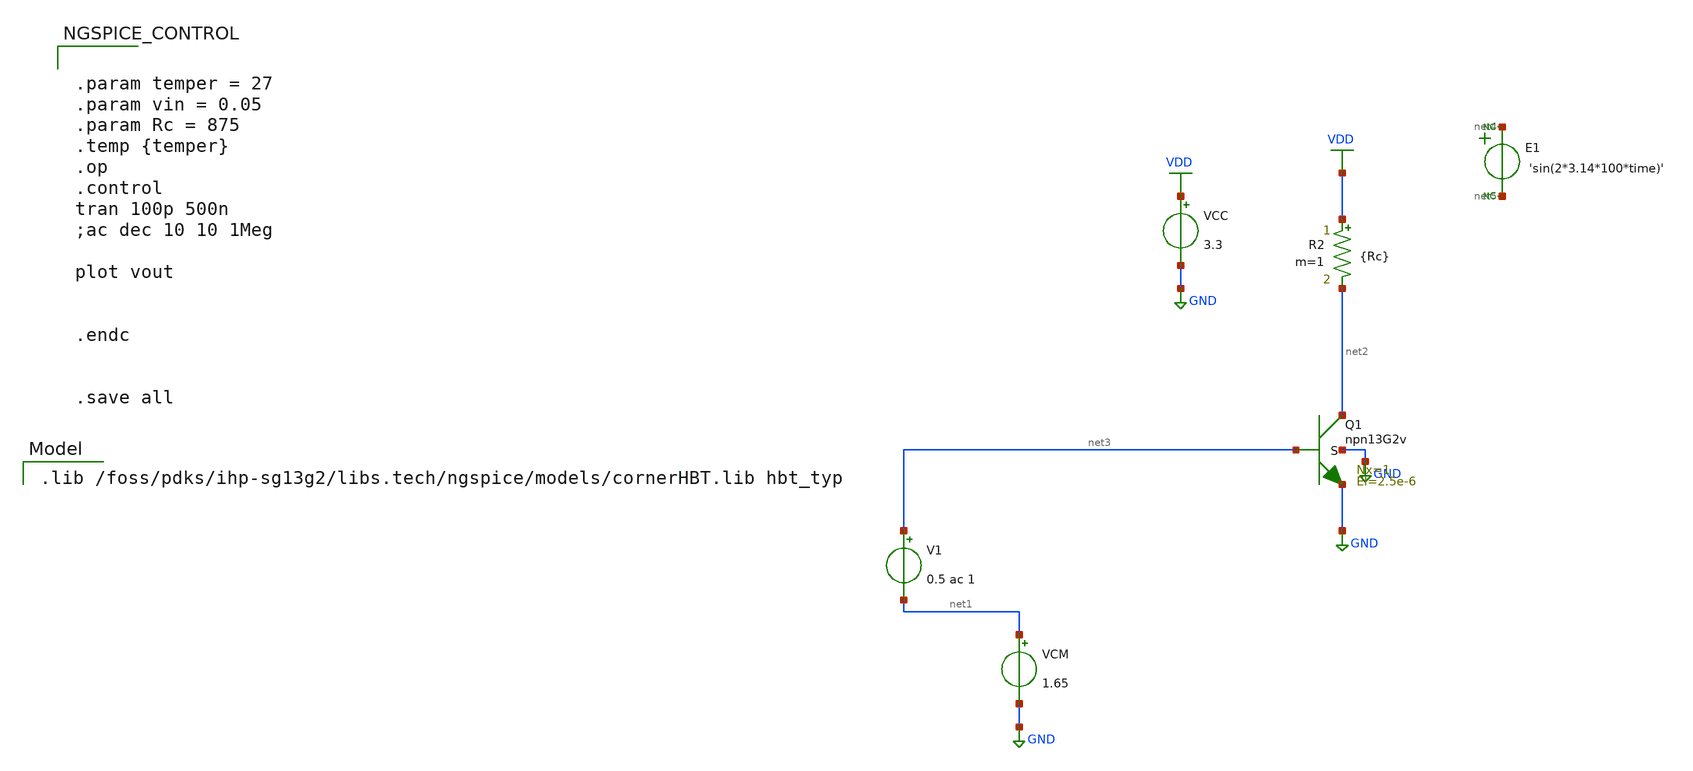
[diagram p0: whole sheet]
** sch_path: data_simu/simulations/LNA_design_ihp_test.sch
**.subckt LNA_design_ihp_test
VCC VDD GND 3.3
R2 VDD net2 {Rc} m=1
VCM net1 GND 1.65
E1 net4 net5 VOL=' 'sin(2*3.14*100*time)' '
* noconn #net4
* noconn #net5
V1 net3 net1 0.5 ac 1
XQ1 net2 net3 GND GND npn13G2v Nx=1 El=2.5e-6 mm_ok=1
**** begin user architecture code

.lib /foss/pdks/ihp-sg13g2/libs.tech/ngspice/models/cornerHBT.lib hbt_typ



.param temper = 27
.param vin = 0.05
.param Rc = 875
.temp {temper}
.op
.control
tran 100p 500n
;ac dec 10 10 1Meg

plot vout


.endc


.save all


**** end user architecture code
**.ends
.GLOBAL GND
.GLOBAL VDD
.end
